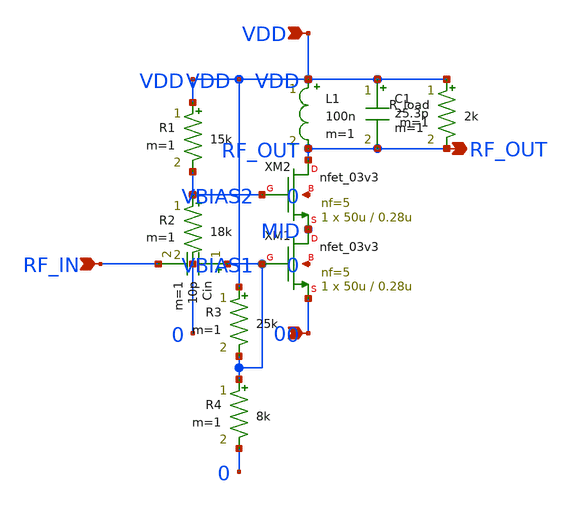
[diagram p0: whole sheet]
** sch_path: modules/PandaChip/designs/rf_trans/lna.sch
**.subckt lna VDD RF_IN RF_OUT 0
*.ipin VDD
*.ipin RF_IN
*.opin RF_OUT
*.ipin 0
XM1 MID VBIAS1 0 0 nfet_03v3 L=0.28u W=50u nf=5 ad='int((nf+1)/2) * W/nf * 0.18u' as='int((nf+2)/2) * W/nf * 0.18u'
+ pd='2*int((nf+1)/2) * (W/nf + 0.18u)' ps='2*int((nf+2)/2) * (W/nf + 0.18u)' nrd='0.18u / W' nrs='0.18u / W'
+ sa=0 sb=0 sd=0 m=1
XM2 RF_OUT VBIAS2 MID 0 nfet_03v3 L=0.28u W=50u nf=5 ad='int((nf+1)/2) * W/nf * 0.18u' as='int((nf+2)/2) * W/nf * 0.18u'
+ pd='2*int((nf+1)/2) * (W/nf + 0.18u)' ps='2*int((nf+2)/2) * (W/nf + 0.18u)' nrd='0.18u / W' nrs='0.18u / W'
+ sa=0 sb=0 sd=0 m=1
L1 VDD RF_OUT 100n m=1
C1 VDD RF_OUT 25.3p m=1
R_load VDD RF_OUT 2k m=1
Cin VBIAS1 RF_IN 10p m=1
R1 VDD VBIAS2 15k m=1
R2 VBIAS2 0 18k m=1
R3 VDD VBIAS1 25k m=1
R4 VBIAS1 0 8k m=1
**.ends
.end
